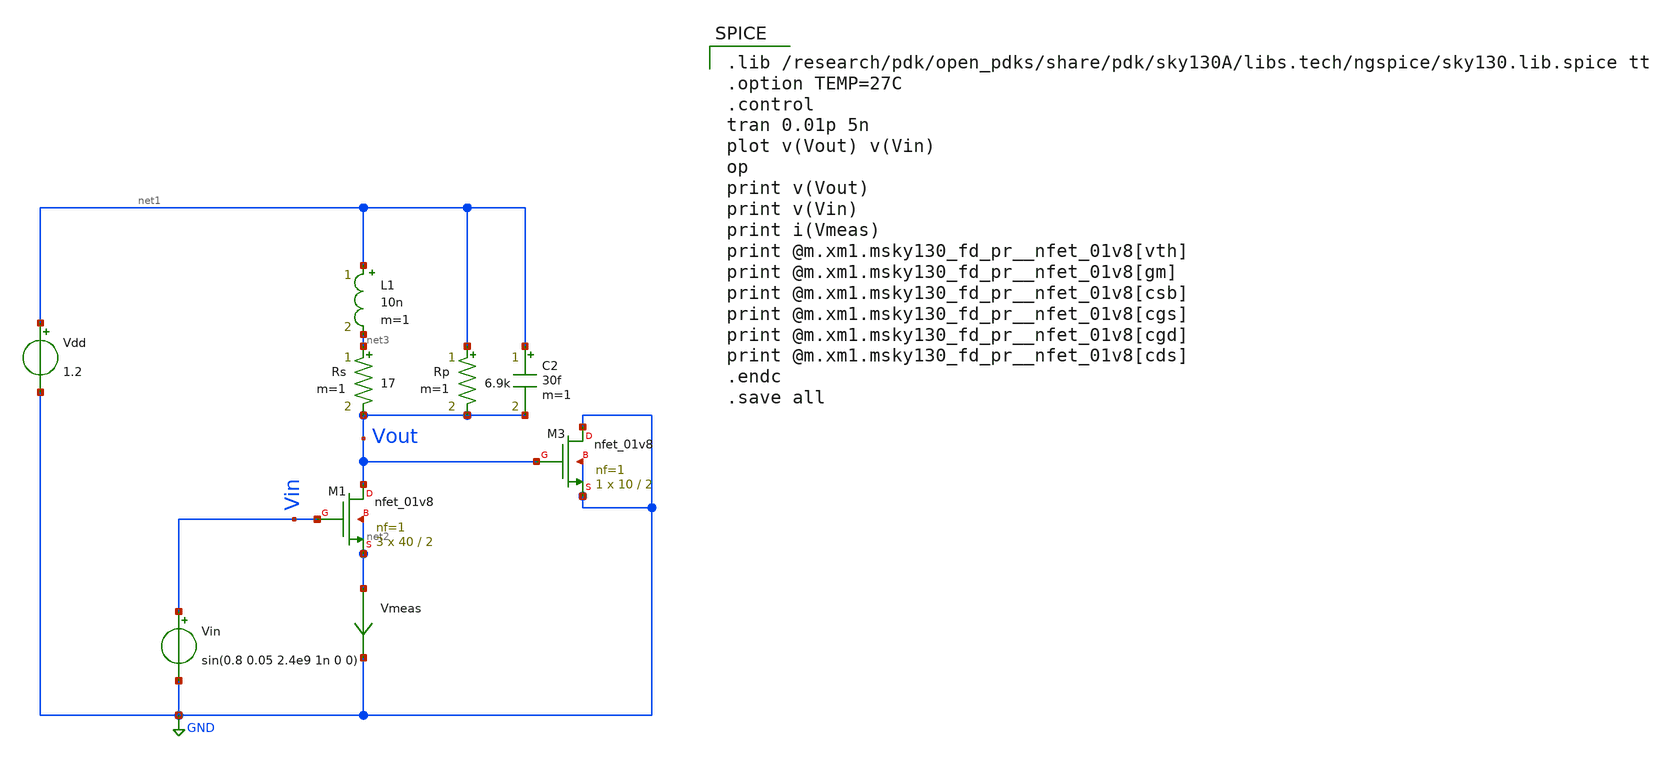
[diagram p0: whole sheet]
** sch_path: skywater_stuff/ECE631_RF_CMOS/LNA.sch
**.subckt LNA
XM1 Vout Vin net2 net2 sky130_fd_pr__nfet_01v8 L=2 W=40 nf=1 ad='int((nf+1)/2) * W/nf * 0.29' as='int((nf+2)/2) * W/nf * 0.29'
+ pd='2*int((nf+1)/2) * (W/nf + 0.29)' ps='2*int((nf+2)/2) * (W/nf + 0.29)' nrd='0.29 / W' nrs='0.29 / W'
+ sa=0 sb=0 sd=0 mult=3 m=3
L1 net1 net3 10n m=1
Vdd net1 GND 1.2
Rp net1 Vout 6.9k m=1
Rs net3 Vout 17 m=1
C2 net1 Vout 30f m=1
Vin Vin GND sin(0.8 0.05 2.4e9 1n 0 0)
Vmeas net2 GND 0
.save i(vmeas)
XM3 GND Vout GND GND sky130_fd_pr__nfet_01v8 L=2 W=10 nf=1 ad='int((nf+1)/2) * W/nf * 0.29' as='int((nf+2)/2) * W/nf * 0.29'
+ pd='2*int((nf+1)/2) * (W/nf + 0.29)' ps='2*int((nf+2)/2) * (W/nf + 0.29)' nrd='0.29 / W' nrs='0.29 / W'
+ sa=0 sb=0 sd=0 mult=1 m=1
**** begin user architecture code

.lib /research/pdk/open_pdks/share/pdk/sky130A/libs.tech/ngspice/sky130.lib.spice tt
.option TEMP=27C
.control
tran 0.01p 5n
plot v(Vout) v(Vin)
op
print v(Vout)
print v(Vin)
print i(Vmeas)
print @m.xm1.msky130_fd_pr__nfet_01v8[vth]
print @m.xm1.msky130_fd_pr__nfet_01v8[gm]
print @m.xm1.msky130_fd_pr__nfet_01v8[csb]
print @m.xm1.msky130_fd_pr__nfet_01v8[cgs]
print @m.xm1.msky130_fd_pr__nfet_01v8[cgd]
print @m.xm1.msky130_fd_pr__nfet_01v8[cds]
.endc
.save all

**** end user architecture code
**.ends
.GLOBAL GND
.end
